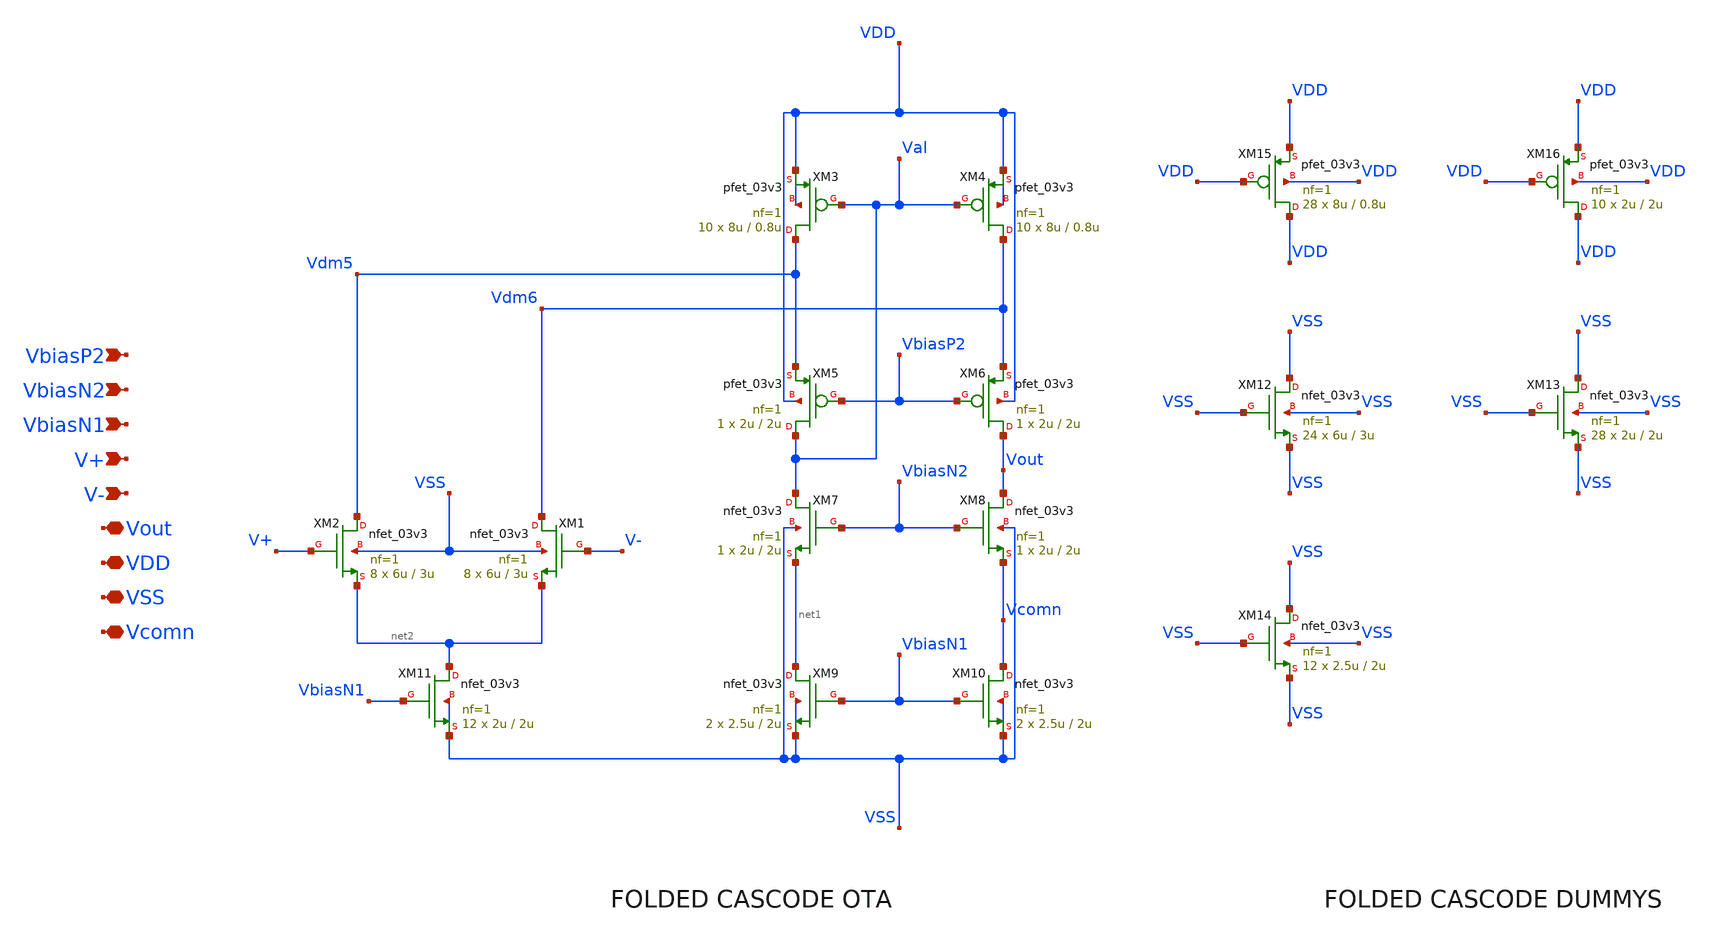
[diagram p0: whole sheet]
** sch_path: designs/gf180/error_amplifier_N_input_core_v2/xschem/error_amplifier_N_input_core_v2.sch
**.subckt error_amplifier_N_input_core_v2 VbiasN2 VDD VbiasP2 VbiasN1 V+ V- VSS Vcomn Vout
*.ipin VbiasN2
*.iopin VDD
*.ipin VbiasP2
*.ipin VbiasN1
*.ipin V+
*.ipin V-
*.iopin VSS
*.iopin Vcomn
*.iopin Vout
XM4 Vdm6 Val VDD VDD pfet_03v3 L=0.8u W=8u nf=1 ad='int((nf+1)/2) * W/nf * 0.18u' as='int((nf+2)/2) * W/nf * 0.18u'
+ pd='2*int((nf+1)/2) * (W/nf + 0.18u)' ps='2*int((nf+2)/2) * (W/nf + 0.18u)' nrd='0.18u / W' nrs='0.18u / W'
+ sa=0 sb=0 sd=0 m=10
XM3 Vdm5 Val VDD VDD pfet_03v3 L=0.8u W=8u nf=1 ad='int((nf+1)/2) * W/nf * 0.18u' as='int((nf+2)/2) * W/nf * 0.18u'
+ pd='2*int((nf+1)/2) * (W/nf + 0.18u)' ps='2*int((nf+2)/2) * (W/nf + 0.18u)' nrd='0.18u / W' nrs='0.18u / W'
+ sa=0 sb=0 sd=0 m=10
XM5 Val VbiasP2 Vdm5 VDD pfet_03v3 L=2u W=2u nf=1 ad='int((nf+1)/2) * W/nf * 0.18u' as='int((nf+2)/2) * W/nf * 0.18u'
+ pd='2*int((nf+1)/2) * (W/nf + 0.18u)' ps='2*int((nf+2)/2) * (W/nf + 0.18u)' nrd='0.18u / W' nrs='0.18u / W'
+ sa=0 sb=0 sd=0 m=1
XM6 Vout VbiasP2 Vdm6 VDD pfet_03v3 L=2u W=2u nf=1 ad='int((nf+1)/2) * W/nf * 0.18u' as='int((nf+2)/2) * W/nf * 0.18u'
+ pd='2*int((nf+1)/2) * (W/nf + 0.18u)' ps='2*int((nf+2)/2) * (W/nf + 0.18u)' nrd='0.18u / W' nrs='0.18u / W'
+ sa=0 sb=0 sd=0 m=1
XM9 net1 VbiasN1 VSS VSS nfet_03v3 L=2u W=2.5u nf=1 ad='int((nf+1)/2) * W/nf * 0.18u' as='int((nf+2)/2) * W/nf * 0.18u'
+ pd='2*int((nf+1)/2) * (W/nf + 0.18u)' ps='2*int((nf+2)/2) * (W/nf + 0.18u)' nrd='0.18u / W' nrs='0.18u / W'
+ sa=0 sb=0 sd=0 m=2
XM8 Vout VbiasN2 Vcomn VSS nfet_03v3 L=2u W=2u nf=1 ad='int((nf+1)/2) * W/nf * 0.18u' as='int((nf+2)/2) * W/nf * 0.18u'
+ pd='2*int((nf+1)/2) * (W/nf + 0.18u)' ps='2*int((nf+2)/2) * (W/nf + 0.18u)' nrd='0.18u / W' nrs='0.18u / W'
+ sa=0 sb=0 sd=0 m=1
XM7 Val VbiasN2 net1 VSS nfet_03v3 L=2u W=2u nf=1 ad='int((nf+1)/2) * W/nf * 0.18u' as='int((nf+2)/2) * W/nf * 0.18u'
+ pd='2*int((nf+1)/2) * (W/nf + 0.18u)' ps='2*int((nf+2)/2) * (W/nf + 0.18u)' nrd='0.18u / W' nrs='0.18u / W'
+ sa=0 sb=0 sd=0 m=1
XM10 Vcomn VbiasN1 VSS VSS nfet_03v3 L=2u W=2.5u nf=1 ad='int((nf+1)/2) * W/nf * 0.18u' as='int((nf+2)/2) * W/nf * 0.18u'
+ pd='2*int((nf+1)/2) * (W/nf + 0.18u)' ps='2*int((nf+2)/2) * (W/nf + 0.18u)' nrd='0.18u / W' nrs='0.18u / W'
+ sa=0 sb=0 sd=0 m=2
XM15 VDD VDD VDD VDD pfet_03v3 L=0.8u W=8u nf=1 ad='int((nf+1)/2) * W/nf * 0.18u' as='int((nf+2)/2) * W/nf * 0.18u'
+ pd='2*int((nf+1)/2) * (W/nf + 0.18u)' ps='2*int((nf+2)/2) * (W/nf + 0.18u)' nrd='0.18u / W' nrs='0.18u / W'
+ sa=0 sb=0 sd=0 m=28
XM16 VDD VDD VDD VDD pfet_03v3 L=2u W=2u nf=1 ad='int((nf+1)/2) * W/nf * 0.18u' as='int((nf+2)/2) * W/nf * 0.18u'
+ pd='2*int((nf+1)/2) * (W/nf + 0.18u)' ps='2*int((nf+2)/2) * (W/nf + 0.18u)' nrd='0.18u / W' nrs='0.18u / W'
+ sa=0 sb=0 sd=0 m=10
XM13 VSS VSS VSS VSS nfet_03v3 L=2u W=2u nf=1 ad='int((nf+1)/2) * W/nf * 0.18u' as='int((nf+2)/2) * W/nf * 0.18u'
+ pd='2*int((nf+1)/2) * (W/nf + 0.18u)' ps='2*int((nf+2)/2) * (W/nf + 0.18u)' nrd='0.18u / W' nrs='0.18u / W'
+ sa=0 sb=0 sd=0 m=28
XM12 VSS VSS VSS VSS nfet_03v3 L=3u W=6u nf=1 ad='int((nf+1)/2) * W/nf * 0.18u' as='int((nf+2)/2) * W/nf * 0.18u'
+ pd='2*int((nf+1)/2) * (W/nf + 0.18u)' ps='2*int((nf+2)/2) * (W/nf + 0.18u)' nrd='0.18u / W' nrs='0.18u / W'
+ sa=0 sb=0 sd=0 m=24
XM14 VSS VSS VSS VSS nfet_03v3 L=2u W=2.5u nf=1 ad='int((nf+1)/2) * W/nf * 0.18u' as='int((nf+2)/2) * W/nf * 0.18u'
+ pd='2*int((nf+1)/2) * (W/nf + 0.18u)' ps='2*int((nf+2)/2) * (W/nf + 0.18u)' nrd='0.18u / W' nrs='0.18u / W'
+ sa=0 sb=0 sd=0 m=12
XM1 Vdm6 V- net2 VSS nfet_03v3 L=3u W=6u nf=1 ad='int((nf+1)/2) * W/nf * 0.18u' as='int((nf+2)/2) * W/nf * 0.18u'
+ pd='2*int((nf+1)/2) * (W/nf + 0.18u)' ps='2*int((nf+2)/2) * (W/nf + 0.18u)' nrd='0.18u / W' nrs='0.18u / W'
+ sa=0 sb=0 sd=0 m=8
XM2 Vdm5 V+ net2 VSS nfet_03v3 L=3u W=6u nf=1 ad='int((nf+1)/2) * W/nf * 0.18u' as='int((nf+2)/2) * W/nf * 0.18u'
+ pd='2*int((nf+1)/2) * (W/nf + 0.18u)' ps='2*int((nf+2)/2) * (W/nf + 0.18u)' nrd='0.18u / W' nrs='0.18u / W'
+ sa=0 sb=0 sd=0 m=8
XM11 net2 VbiasN1 VSS VSS nfet_03v3 L=2u W=2u nf=1 ad='int((nf+1)/2) * W/nf * 0.18u' as='int((nf+2)/2) * W/nf * 0.18u'
+ pd='2*int((nf+1)/2) * (W/nf + 0.18u)' ps='2*int((nf+2)/2) * (W/nf + 0.18u)' nrd='0.18u / W' nrs='0.18u / W'
+ sa=0 sb=0 sd=0 m=12
**.ends
.end
